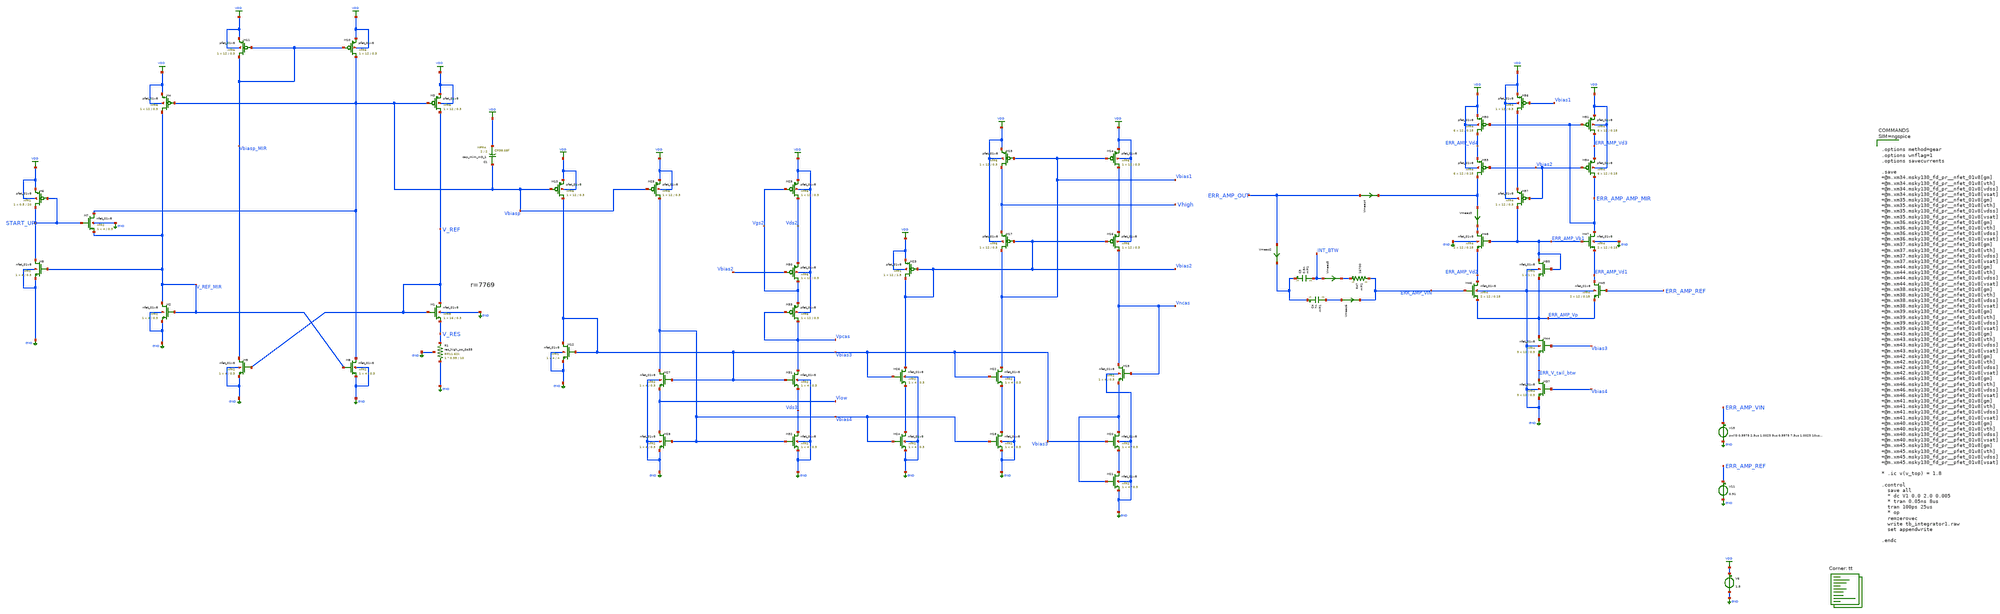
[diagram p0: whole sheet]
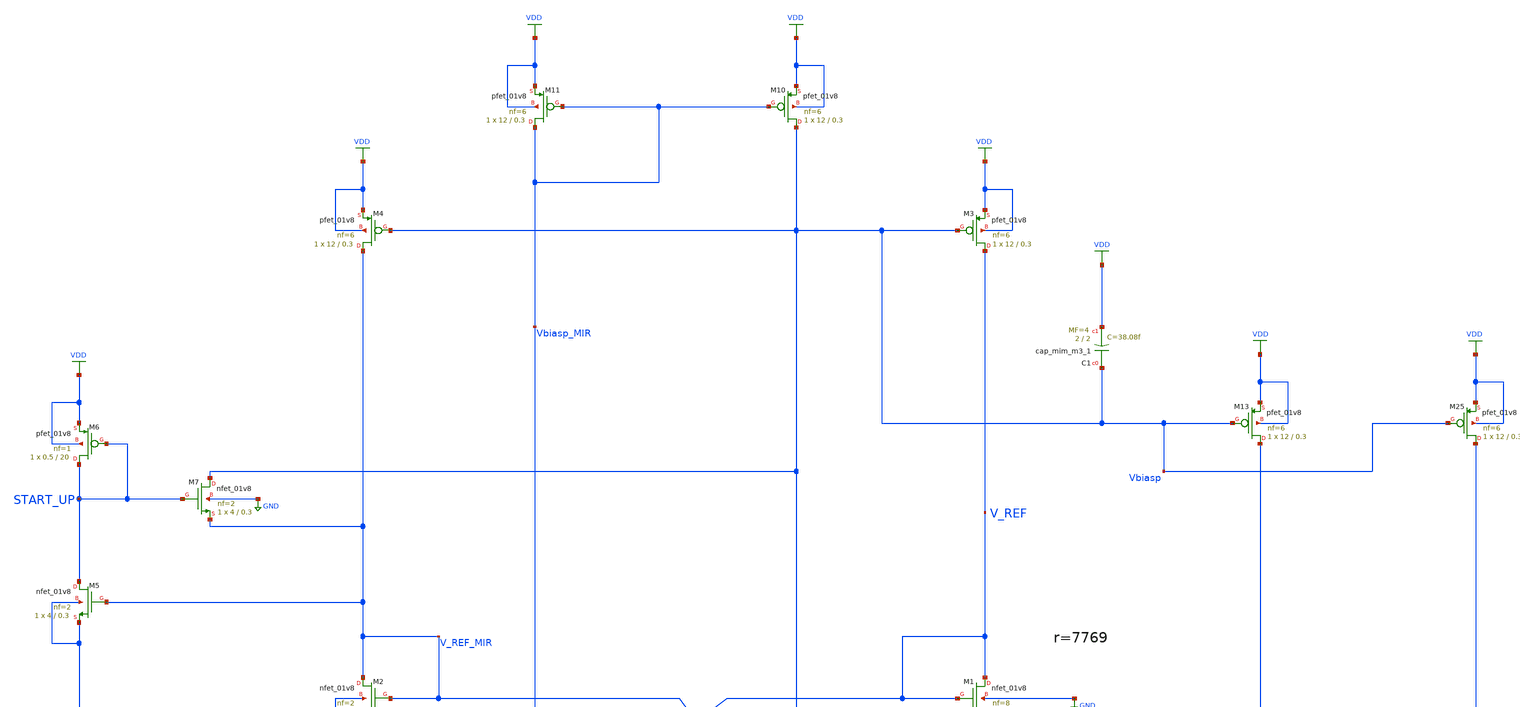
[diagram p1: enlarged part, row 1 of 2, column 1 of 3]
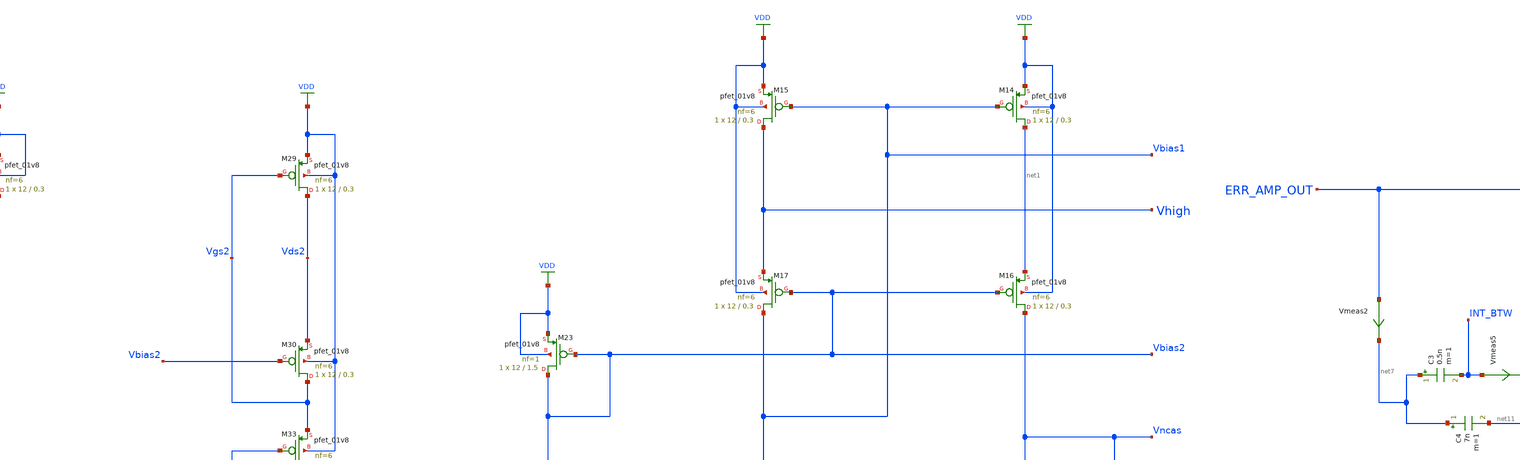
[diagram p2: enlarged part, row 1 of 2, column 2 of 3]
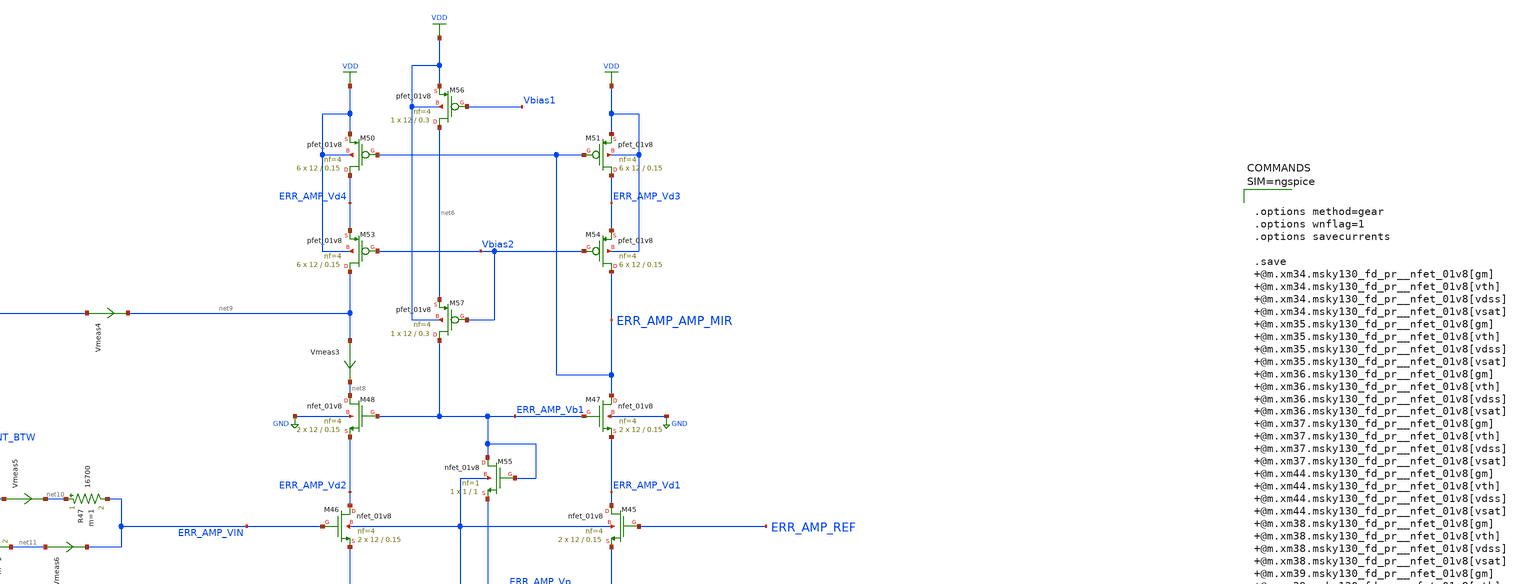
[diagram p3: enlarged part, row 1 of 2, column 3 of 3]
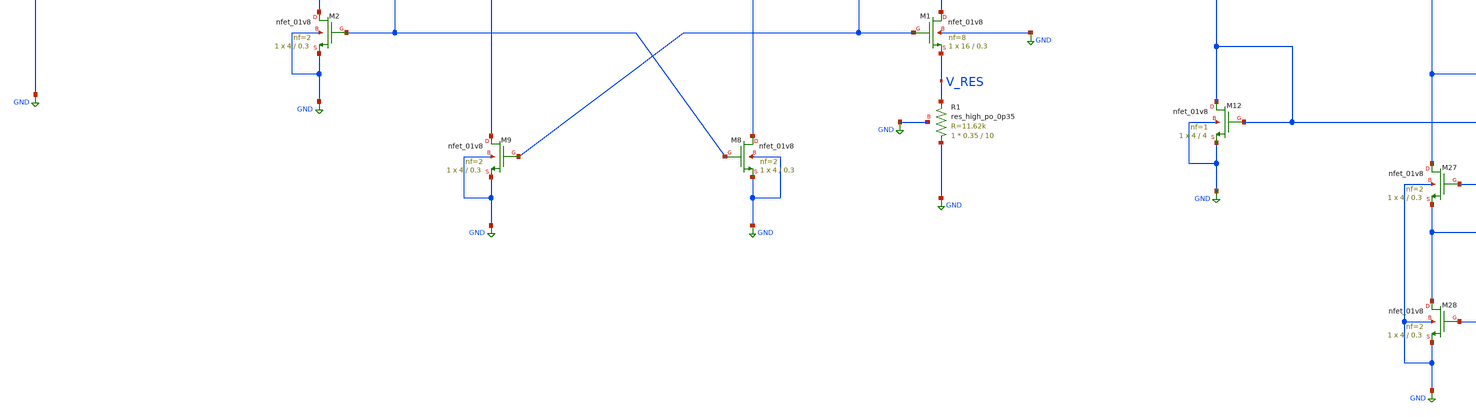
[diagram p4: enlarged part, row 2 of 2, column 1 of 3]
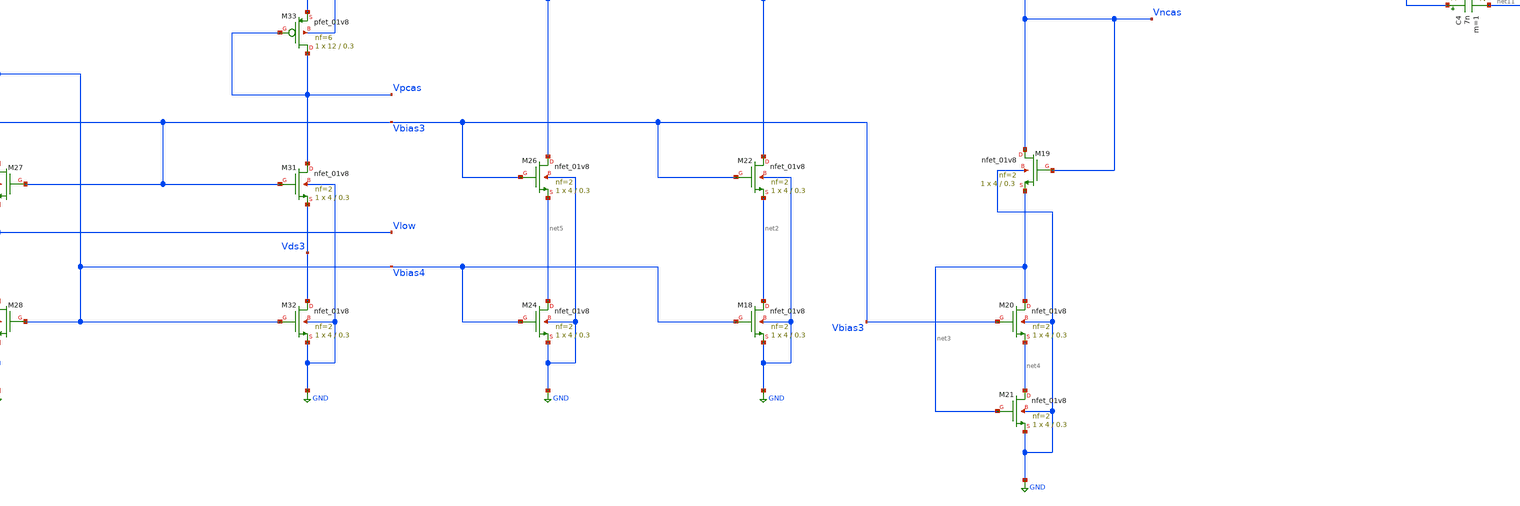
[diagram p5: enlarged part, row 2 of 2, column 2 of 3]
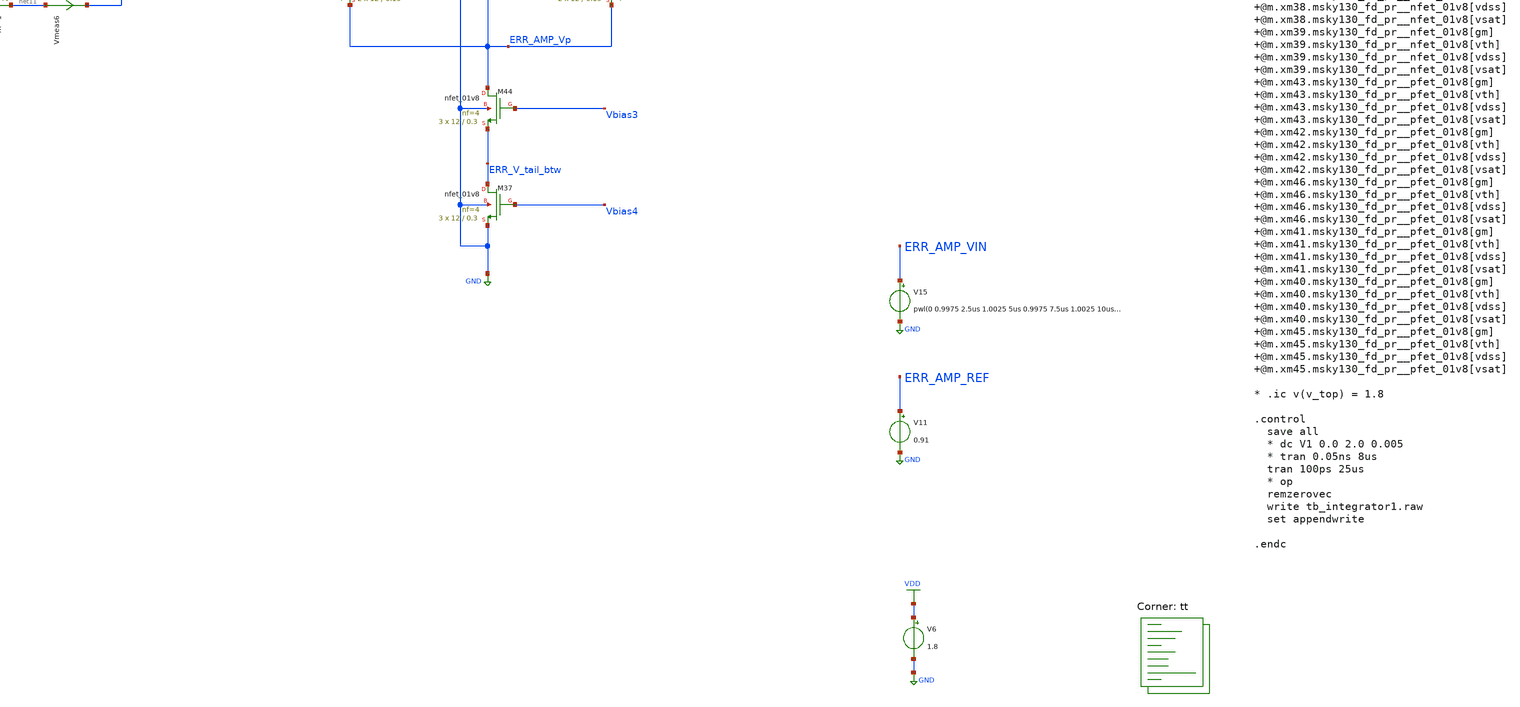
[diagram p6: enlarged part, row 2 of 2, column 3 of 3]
** sch_path: projects/ASU/EEE572/schematic/tb_integrator1.sch
**.subckt tb_integrator1
V6 VDD GND 1.8
XM1 V_REF V_REF V_RES GND sky130_fd_pr__nfet_01v8 L=0.3 W=16 nf=8 ad='int((nf+1)/2) * W/nf * 0.29' as='int((nf+2)/2) * W/nf * 0.29'
+ pd='2*int((nf+1)/2) * (W/nf + 0.29)' ps='2*int((nf+2)/2) * (W/nf + 0.29)' nrd='0.29 / W' nrs='0.29 / W'
+ sa=0 sb=0 sd=0 mult=1 m=1
XM2 V_REF_MIR V_REF_MIR GND GND sky130_fd_pr__nfet_01v8 L=0.3 W=4 nf=2 ad='int((nf+1)/2) * W/nf * 0.29'
+ as='int((nf+2)/2) * W/nf * 0.29' pd='2*int((nf+1)/2) * (W/nf + 0.29)' ps='2*int((nf+2)/2) * (W/nf + 0.29)'
+ nrd='0.29 / W' nrs='0.29 / W' sa=0 sb=0 sd=0 mult=1 m=1
XM5 START_UP V_REF_MIR GND GND sky130_fd_pr__nfet_01v8 L=0.3 W=4 nf=2 ad='int((nf+1)/2) * W/nf * 0.29'
+ as='int((nf+2)/2) * W/nf * 0.29' pd='2*int((nf+1)/2) * (W/nf + 0.29)' ps='2*int((nf+2)/2) * (W/nf + 0.29)'
+ nrd='0.29 / W' nrs='0.29 / W' sa=0 sb=0 sd=0 mult=1 m=1
XM7 Vbiasp START_UP V_REF_MIR GND sky130_fd_pr__nfet_01v8 L=0.3 W=4 nf=2 ad='int((nf+1)/2) * W/nf * 0.29'
+ as='int((nf+2)/2) * W/nf * 0.29' pd='2*int((nf+1)/2) * (W/nf + 0.29)' ps='2*int((nf+2)/2) * (W/nf + 0.29)'
+ nrd='0.29 / W' nrs='0.29 / W' sa=0 sb=0 sd=0 mult=1 m=1
XM6 START_UP START_UP VDD VDD sky130_fd_pr__pfet_01v8 L=20 W=0.5 nf=1 ad='int((nf+1)/2) * W/nf * 0.29'
+ as='int((nf+2)/2) * W/nf * 0.29' pd='2*int((nf+1)/2) * (W/nf + 0.29)' ps='2*int((nf+2)/2) * (W/nf + 0.29)'
+ nrd='0.29 / W' nrs='0.29 / W' sa=0 sb=0 sd=0 mult=1 m=1
XM3 V_REF Vbiasp VDD VDD sky130_fd_pr__pfet_01v8 L=0.3 W=12 nf=6 ad='int((nf+1)/2) * W/nf * 0.29' as='int((nf+2)/2) * W/nf * 0.29'
+ pd='2*int((nf+1)/2) * (W/nf + 0.29)' ps='2*int((nf+2)/2) * (W/nf + 0.29)' nrd='0.29 / W' nrs='0.29 / W'
+ sa=0 sb=0 sd=0 mult=1 m=1
XM4 V_REF_MIR Vbiasp VDD VDD sky130_fd_pr__pfet_01v8 L=0.3 W=12 nf=6 ad='int((nf+1)/2) * W/nf * 0.29'
+ as='int((nf+2)/2) * W/nf * 0.29' pd='2*int((nf+1)/2) * (W/nf + 0.29)' ps='2*int((nf+2)/2) * (W/nf + 0.29)'
+ nrd='0.29 / W' nrs='0.29 / W' sa=0 sb=0 sd=0 mult=1 m=1
XM8 Vbiasp V_REF_MIR GND GND sky130_fd_pr__nfet_01v8 L=0.3 W=4 nf=2 ad='int((nf+1)/2) * W/nf * 0.29'
+ as='int((nf+2)/2) * W/nf * 0.29' pd='2*int((nf+1)/2) * (W/nf + 0.29)' ps='2*int((nf+2)/2) * (W/nf + 0.29)'
+ nrd='0.29 / W' nrs='0.29 / W' sa=0 sb=0 sd=0 mult=1 m=1
XM9 Vbiasp_MIR V_REF GND GND sky130_fd_pr__nfet_01v8 L=0.3 W=4 nf=2 ad='int((nf+1)/2) * W/nf * 0.29'
+ as='int((nf+2)/2) * W/nf * 0.29' pd='2*int((nf+1)/2) * (W/nf + 0.29)' ps='2*int((nf+2)/2) * (W/nf + 0.29)'
+ nrd='0.29 / W' nrs='0.29 / W' sa=0 sb=0 sd=0 mult=1 m=1
XM10 Vbiasp Vbiasp_MIR VDD VDD sky130_fd_pr__pfet_01v8 L=0.3 W=12 nf=6 ad='int((nf+1)/2) * W/nf * 0.29'
+ as='int((nf+2)/2) * W/nf * 0.29' pd='2*int((nf+1)/2) * (W/nf + 0.29)' ps='2*int((nf+2)/2) * (W/nf + 0.29)'
+ nrd='0.29 / W' nrs='0.29 / W' sa=0 sb=0 sd=0 mult=1 m=1
XM11 Vbiasp_MIR Vbiasp_MIR VDD VDD sky130_fd_pr__pfet_01v8 L=0.3 W=12 nf=6 ad='int((nf+1)/2) * W/nf * 0.29'
+ as='int((nf+2)/2) * W/nf * 0.29' pd='2*int((nf+1)/2) * (W/nf + 0.29)' ps='2*int((nf+2)/2) * (W/nf + 0.29)'
+ nrd='0.29 / W' nrs='0.29 / W' sa=0 sb=0 sd=0 mult=1 m=1
XM12 Vbias3 Vbias3 GND GND sky130_fd_pr__nfet_01v8 L=4 W=4 nf=1 ad='int((nf+1)/2) * W/nf * 0.29' as='int((nf+2)/2) * W/nf * 0.29'
+ pd='2*int((nf+1)/2) * (W/nf + 0.29)' ps='2*int((nf+2)/2) * (W/nf + 0.29)' nrd='0.29 / W' nrs='0.29 / W'
+ sa=0 sb=0 sd=0 mult=1 m=1
XM13 Vbias3 Vbiasp VDD VDD sky130_fd_pr__pfet_01v8 L=0.3 W=12 nf=6 ad='int((nf+1)/2) * W/nf * 0.29' as='int((nf+2)/2) * W/nf * 0.29'
+ pd='2*int((nf+1)/2) * (W/nf + 0.29)' ps='2*int((nf+2)/2) * (W/nf + 0.29)' nrd='0.29 / W' nrs='0.29 / W'
+ sa=0 sb=0 sd=0 mult=1 m=1
XM14 net1 Vbias1 VDD VDD sky130_fd_pr__pfet_01v8 L=0.3 W=12 nf=6 ad='int((nf+1)/2) * W/nf * 0.29' as='int((nf+2)/2) * W/nf * 0.29'
+ pd='2*int((nf+1)/2) * (W/nf + 0.29)' ps='2*int((nf+2)/2) * (W/nf + 0.29)' nrd='0.29 / W' nrs='0.29 / W'
+ sa=0 sb=0 sd=0 mult=1 m=1
XM15 Vhigh Vbias1 VDD VDD sky130_fd_pr__pfet_01v8 L=0.3 W=12 nf=6 ad='int((nf+1)/2) * W/nf * 0.29' as='int((nf+2)/2) * W/nf * 0.29'
+ pd='2*int((nf+1)/2) * (W/nf + 0.29)' ps='2*int((nf+2)/2) * (W/nf + 0.29)' nrd='0.29 / W' nrs='0.29 / W'
+ sa=0 sb=0 sd=0 mult=1 m=1
XM16 Vncas Vbias2 net1 VDD sky130_fd_pr__pfet_01v8 L=0.3 W=12 nf=6 ad='int((nf+1)/2) * W/nf * 0.29' as='int((nf+2)/2) * W/nf * 0.29'
+ pd='2*int((nf+1)/2) * (W/nf + 0.29)' ps='2*int((nf+2)/2) * (W/nf + 0.29)' nrd='0.29 / W' nrs='0.29 / W'
+ sa=0 sb=0 sd=0 mult=1 m=1
XM17 Vbias1 Vbias2 Vhigh VDD sky130_fd_pr__pfet_01v8 L=0.3 W=12 nf=6 ad='int((nf+1)/2) * W/nf * 0.29'
+ as='int((nf+2)/2) * W/nf * 0.29' pd='2*int((nf+1)/2) * (W/nf + 0.29)' ps='2*int((nf+2)/2) * (W/nf + 0.29)'
+ nrd='0.29 / W' nrs='0.29 / W' sa=0 sb=0 sd=0 mult=1 m=1
XM18 net2 Vbias4 GND GND sky130_fd_pr__nfet_01v8 L=0.3 W=4 nf=2 ad='int((nf+1)/2) * W/nf * 0.29' as='int((nf+2)/2) * W/nf * 0.29'
+ pd='2*int((nf+1)/2) * (W/nf + 0.29)' ps='2*int((nf+2)/2) * (W/nf + 0.29)' nrd='0.29 / W' nrs='0.29 / W'
+ sa=0 sb=0 sd=0 mult=1 m=1
XM19 Vncas Vncas net3 GND sky130_fd_pr__nfet_01v8 L=0.3 W=4 nf=2 ad='int((nf+1)/2) * W/nf * 0.29' as='int((nf+2)/2) * W/nf * 0.29'
+ pd='2*int((nf+1)/2) * (W/nf + 0.29)' ps='2*int((nf+2)/2) * (W/nf + 0.29)' nrd='0.29 / W' nrs='0.29 / W'
+ sa=0 sb=0 sd=0 mult=1 m=1
XM20 net3 Vbias3 net4 GND sky130_fd_pr__nfet_01v8 L=0.3 W=4 nf=2 ad='int((nf+1)/2) * W/nf * 0.29' as='int((nf+2)/2) * W/nf * 0.29'
+ pd='2*int((nf+1)/2) * (W/nf + 0.29)' ps='2*int((nf+2)/2) * (W/nf + 0.29)' nrd='0.29 / W' nrs='0.29 / W'
+ sa=0 sb=0 sd=0 mult=1 m=1
XM21 net4 net3 GND GND sky130_fd_pr__nfet_01v8 L=0.3 W=4 nf=2 ad='int((nf+1)/2) * W/nf * 0.29' as='int((nf+2)/2) * W/nf * 0.29'
+ pd='2*int((nf+1)/2) * (W/nf + 0.29)' ps='2*int((nf+2)/2) * (W/nf + 0.29)' nrd='0.29 / W' nrs='0.29 / W'
+ sa=0 sb=0 sd=0 mult=1 m=1
XM25 Vbias4 Vbiasp VDD VDD sky130_fd_pr__pfet_01v8 L=0.3 W=12 nf=6 ad='int((nf+1)/2) * W/nf * 0.29' as='int((nf+2)/2) * W/nf * 0.29'
+ pd='2*int((nf+1)/2) * (W/nf + 0.29)' ps='2*int((nf+2)/2) * (W/nf + 0.29)' nrd='0.29 / W' nrs='0.29 / W'
+ sa=0 sb=0 sd=0 mult=1 m=1
XM27 Vbias4 Vbias3 Vlow GND sky130_fd_pr__nfet_01v8 L=0.3 W=4 nf=2 ad='int((nf+1)/2) * W/nf * 0.29' as='int((nf+2)/2) * W/nf * 0.29'
+ pd='2*int((nf+1)/2) * (W/nf + 0.29)' ps='2*int((nf+2)/2) * (W/nf + 0.29)' nrd='0.29 / W' nrs='0.29 / W'
+ sa=0 sb=0 sd=0 mult=1 m=1
XM28 Vlow Vbias4 GND GND sky130_fd_pr__nfet_01v8 L=0.3 W=4 nf=2 ad='int((nf+1)/2) * W/nf * 0.29' as='int((nf+2)/2) * W/nf * 0.29'
+ pd='2*int((nf+1)/2) * (W/nf + 0.29)' ps='2*int((nf+2)/2) * (W/nf + 0.29)' nrd='0.29 / W' nrs='0.29 / W'
+ sa=0 sb=0 sd=0 mult=1 m=1
XM29 Vds2 Vgs2 VDD VDD sky130_fd_pr__pfet_01v8 L=0.3 W=12 nf=6 ad='int((nf+1)/2) * W/nf * 0.29' as='int((nf+2)/2) * W/nf * 0.29'
+ pd='2*int((nf+1)/2) * (W/nf + 0.29)' ps='2*int((nf+2)/2) * (W/nf + 0.29)' nrd='0.29 / W' nrs='0.29 / W'
+ sa=0 sb=0 sd=0 mult=1 m=1
XM30 Vgs2 Vbias2 Vds2 VDD sky130_fd_pr__pfet_01v8 L=0.3 W=12 nf=6 ad='int((nf+1)/2) * W/nf * 0.29' as='int((nf+2)/2) * W/nf * 0.29'
+ pd='2*int((nf+1)/2) * (W/nf + 0.29)' ps='2*int((nf+2)/2) * (W/nf + 0.29)' nrd='0.29 / W' nrs='0.29 / W'
+ sa=0 sb=0 sd=0 mult=1 m=1
XM31 Vpcas Vbias3 Vds3 GND sky130_fd_pr__nfet_01v8 L=0.3 W=4 nf=2 ad='int((nf+1)/2) * W/nf * 0.29' as='int((nf+2)/2) * W/nf * 0.29'
+ pd='2*int((nf+1)/2) * (W/nf + 0.29)' ps='2*int((nf+2)/2) * (W/nf + 0.29)' nrd='0.29 / W' nrs='0.29 / W'
+ sa=0 sb=0 sd=0 mult=1 m=1
XM32 Vds3 Vbias4 GND GND sky130_fd_pr__nfet_01v8 L=0.3 W=4 nf=2 ad='int((nf+1)/2) * W/nf * 0.29' as='int((nf+2)/2) * W/nf * 0.29'
+ pd='2*int((nf+1)/2) * (W/nf + 0.29)' ps='2*int((nf+2)/2) * (W/nf + 0.29)' nrd='0.29 / W' nrs='0.29 / W'
+ sa=0 sb=0 sd=0 mult=1 m=1
XM33 Vpcas Vpcas Vgs2 VDD sky130_fd_pr__pfet_01v8 L=0.3 W=12 nf=6 ad='int((nf+1)/2) * W/nf * 0.29' as='int((nf+2)/2) * W/nf * 0.29'
+ pd='2*int((nf+1)/2) * (W/nf + 0.29)' ps='2*int((nf+2)/2) * (W/nf + 0.29)' nrd='0.29 / W' nrs='0.29 / W'
+ sa=0 sb=0 sd=0 mult=1 m=1
XM22 Vbias1 Vbias3 net2 GND sky130_fd_pr__nfet_01v8 L=0.3 W=4 nf=2 ad='int((nf+1)/2) * W/nf * 0.29' as='int((nf+2)/2) * W/nf * 0.29'
+ pd='2*int((nf+1)/2) * (W/nf + 0.29)' ps='2*int((nf+2)/2) * (W/nf + 0.29)' nrd='0.29 / W' nrs='0.29 / W'
+ sa=0 sb=0 sd=0 mult=1 m=1
XM23 Vbias2 Vbias2 VDD VDD sky130_fd_pr__pfet_01v8 L=1.5 W=12 nf=1 ad='int((nf+1)/2) * W/nf * 0.29' as='int((nf+2)/2) * W/nf * 0.29'
+ pd='2*int((nf+1)/2) * (W/nf + 0.29)' ps='2*int((nf+2)/2) * (W/nf + 0.29)' nrd='0.29 / W' nrs='0.29 / W'
+ sa=0 sb=0 sd=0 mult=1 m=1
XM24 net5 Vbias4 GND GND sky130_fd_pr__nfet_01v8 L=0.3 W=4 nf=2 ad='int((nf+1)/2) * W/nf * 0.29' as='int((nf+2)/2) * W/nf * 0.29'
+ pd='2*int((nf+1)/2) * (W/nf + 0.29)' ps='2*int((nf+2)/2) * (W/nf + 0.29)' nrd='0.29 / W' nrs='0.29 / W'
+ sa=0 sb=0 sd=0 mult=1 m=1
XM26 Vbias2 Vbias3 net5 GND sky130_fd_pr__nfet_01v8 L=0.3 W=4 nf=2 ad='int((nf+1)/2) * W/nf * 0.29' as='int((nf+2)/2) * W/nf * 0.29'
+ pd='2*int((nf+1)/2) * (W/nf + 0.29)' ps='2*int((nf+2)/2) * (W/nf + 0.29)' nrd='0.29 / W' nrs='0.29 / W'
+ sa=0 sb=0 sd=0 mult=1 m=1
XC1 Vbiasp VDD sky130_fd_pr__cap_mim_m3_1 W=2 L=2 MF=4 m=4
XR1 GND V_RES GND sky130_fd_pr__res_high_po_0p35 L=10 mult=1 m=1
XM37 ERR_V_tail_btw Vbias4 GND GND sky130_fd_pr__nfet_01v8 L=0.3 W=12 nf=4 ad='int((nf+1)/2) * W/nf * 0.29'
+ as='int((nf+2)/2) * W/nf * 0.29' pd='2*int((nf+1)/2) * (W/nf + 0.29)' ps='2*int((nf+2)/2) * (W/nf + 0.29)'
+ nrd='0.29 / W' nrs='0.29 / W' sa=0 sb=0 sd=0 mult=3 m=3
XM44 ERR_AMP_Vp Vbias3 ERR_V_tail_btw GND sky130_fd_pr__nfet_01v8 L=0.3 W=12 nf=4 ad='int((nf+1)/2) * W/nf * 0.29'
+ as='int((nf+2)/2) * W/nf * 0.29' pd='2*int((nf+1)/2) * (W/nf + 0.29)' ps='2*int((nf+2)/2) * (W/nf + 0.29)'
+ nrd='0.29 / W' nrs='0.29 / W' sa=0 sb=0 sd=0 mult=3 m=3
XM45 ERR_AMP_Vd1 ERR_AMP_REF ERR_AMP_Vp GND sky130_fd_pr__nfet_01v8 L=0.15 W=12 nf=4 ad='int((nf+1)/2) * W/nf * 0.29'
+ as='int((nf+2)/2) * W/nf * 0.29' pd='2*int((nf+1)/2) * (W/nf + 0.29)' ps='2*int((nf+2)/2) * (W/nf + 0.29)'
+ nrd='0.29 / W' nrs='0.29 / W' sa=0 sb=0 sd=0 mult=2 m=2
XM46 ERR_AMP_Vd2 ERR_AMP_VIN ERR_AMP_Vp GND sky130_fd_pr__nfet_01v8 L=0.15 W=12 nf=4 ad='int((nf+1)/2) * W/nf * 0.29'
+ as='int((nf+2)/2) * W/nf * 0.29' pd='2*int((nf+1)/2) * (W/nf + 0.29)' ps='2*int((nf+2)/2) * (W/nf + 0.29)'
+ nrd='0.29 / W' nrs='0.29 / W' sa=0 sb=0 sd=0 mult=2 m=2
XM47 ERR_AMP_AMP_MIR ERR_AMP_Vb1 ERR_AMP_Vd1 GND sky130_fd_pr__nfet_01v8 L=0.15 W=12 nf=4 ad='int((nf+1)/2) * W/nf * 0.29'
+ as='int((nf+2)/2) * W/nf * 0.29' pd='2*int((nf+1)/2) * (W/nf + 0.29)' ps='2*int((nf+2)/2) * (W/nf + 0.29)'
+ nrd='0.29 / W' nrs='0.29 / W' sa=0 sb=0 sd=0 mult=2 m=2
XM48 net8 ERR_AMP_Vb1 ERR_AMP_Vd2 GND sky130_fd_pr__nfet_01v8 L=0.15 W=12 nf=4 ad='int((nf+1)/2) * W/nf * 0.29'
+ as='int((nf+2)/2) * W/nf * 0.29' pd='2*int((nf+1)/2) * (W/nf + 0.29)' ps='2*int((nf+2)/2) * (W/nf + 0.29)'
+ nrd='0.29 / W' nrs='0.29 / W' sa=0 sb=0 sd=0 mult=2 m=2
XM50 ERR_AMP_Vd4 ERR_AMP_AMP_MIR VDD VDD sky130_fd_pr__pfet_01v8 L=0.15 W=12 nf=4 ad='int((nf+1)/2) * W/nf * 0.29'
+ as='int((nf+2)/2) * W/nf * 0.29' pd='2*int((nf+1)/2) * (W/nf + 0.29)' ps='2*int((nf+2)/2) * (W/nf + 0.29)'
+ nrd='0.29 / W' nrs='0.29 / W' sa=0 sb=0 sd=0 mult=6 m=6
XM51 ERR_AMP_Vd3 ERR_AMP_AMP_MIR VDD VDD sky130_fd_pr__pfet_01v8 L=0.15 W=12 nf=4 ad='int((nf+1)/2) * W/nf * 0.29'
+ as='int((nf+2)/2) * W/nf * 0.29' pd='2*int((nf+1)/2) * (W/nf + 0.29)' ps='2*int((nf+2)/2) * (W/nf + 0.29)'
+ nrd='0.29 / W' nrs='0.29 / W' sa=0 sb=0 sd=0 mult=6 m=6
XM53 net9 Vbias2 ERR_AMP_Vd4 VDD sky130_fd_pr__pfet_01v8 L=0.15 W=12 nf=4 ad='int((nf+1)/2) * W/nf * 0.29'
+ as='int((nf+2)/2) * W/nf * 0.29' pd='2*int((nf+1)/2) * (W/nf + 0.29)' ps='2*int((nf+2)/2) * (W/nf + 0.29)'
+ nrd='0.29 / W' nrs='0.29 / W' sa=0 sb=0 sd=0 mult=6 m=6
XM54 ERR_AMP_AMP_MIR Vbias2 ERR_AMP_Vd3 VDD sky130_fd_pr__pfet_01v8 L=0.15 W=12 nf=4 ad='int((nf+1)/2) * W/nf * 0.29'
+ as='int((nf+2)/2) * W/nf * 0.29' pd='2*int((nf+1)/2) * (W/nf + 0.29)' ps='2*int((nf+2)/2) * (W/nf + 0.29)'
+ nrd='0.29 / W' nrs='0.29 / W' sa=0 sb=0 sd=0 mult=6 m=6
XM55 ERR_AMP_Vb1 ERR_AMP_Vb1 ERR_AMP_Vp GND sky130_fd_pr__nfet_01v8 L=1 W=1 nf=1 ad='int((nf+1)/2) * W/nf * 0.29'
+ as='int((nf+2)/2) * W/nf * 0.29' pd='2*int((nf+1)/2) * (W/nf + 0.29)' ps='2*int((nf+2)/2) * (W/nf + 0.29)'
+ nrd='0.29 / W' nrs='0.29 / W' sa=0 sb=0 sd=0 mult=1 m=1
XM56 net6 Vbias1 VDD VDD sky130_fd_pr__pfet_01v8 L=0.3 W=12 nf=4 ad='int((nf+1)/2) * W/nf * 0.29' as='int((nf+2)/2) * W/nf * 0.29'
+ pd='2*int((nf+1)/2) * (W/nf + 0.29)' ps='2*int((nf+2)/2) * (W/nf + 0.29)' nrd='0.29 / W' nrs='0.29 / W'
+ sa=0 sb=0 sd=0 mult=1 m=1
XM57 ERR_AMP_Vb1 Vbias2 net6 VDD sky130_fd_pr__pfet_01v8 L=0.3 W=12 nf=4 ad='int((nf+1)/2) * W/nf * 0.29'
+ as='int((nf+2)/2) * W/nf * 0.29' pd='2*int((nf+1)/2) * (W/nf + 0.29)' ps='2*int((nf+2)/2) * (W/nf + 0.29)'
+ nrd='0.29 / W' nrs='0.29 / W' sa=0 sb=0 sd=0 mult=1 m=1
C3 net7 INT_BTW 0.5n m=1
R47 net10 ERR_AMP_VIN 16700 m=1
C4 net7 net11 7n m=1
V11 ERR_AMP_REF GND 0.91
V15 ERR_AMP_VIN GND pwl(0 0.9975 2.5us 1.0025 5us 0.9975 7.5us 1.0025 10us 0.9975 12.5us 1.0025 15us
+ 0.9975 17.5us 1.0025 20us 0.9975 22.5us 1.0025 25us 0.9975)
Vmeas2 ERR_AMP_OUT net7 0
.save i(vmeas2)
Vmeas3 net9 net8 0
.save i(vmeas3)
Vmeas4 ERR_AMP_OUT net9 0
.save i(vmeas4)
Vmeas5 INT_BTW net10 0
.save i(vmeas5)
Vmeas6 net11 ERR_AMP_VIN 0
.save i(vmeas6)
**** begin user architecture code
.lib $::SKYWATER_MODELS/sky130.lib.spice tt



.options method=gear
.options wnflag=1
.options savecurrents

.save @m.xm34.msky130_fd_pr__nfet_01v8[gm] @m.xm34.msky130_fd_pr__nfet_01v8[vth] @m.xm34.msky130_fd_pr__nfet_01v8[vdss] @m.xm34.msky130_fd_pr__nfet_01v8[vsat] @m.xm35.msky130_fd_pr__nfet_01v8[gm] @m.xm35.msky130_fd_pr__nfet_01v8[vth] @m.xm35.msky130_fd_pr__nfet_01v8[vdss] @m.xm35.msky130_fd_pr__nfet_01v8[vsat] @m.xm36.msky130_fd_pr__nfet_01v8[gm] @m.xm36.msky130_fd_pr__nfet_01v8[vth] @m.xm36.msky130_fd_pr__nfet_01v8[vdss] @m.xm36.msky130_fd_pr__nfet_01v8[vsat] @m.xm37.msky130_fd_pr__nfet_01v8[gm] @m.xm37.msky130_fd_pr__nfet_01v8[vth] @m.xm37.msky130_fd_pr__nfet_01v8[vdss] @m.xm37.msky130_fd_pr__nfet_01v8[vsat] @m.xm44.msky130_fd_pr__nfet_01v8[gm] @m.xm44.msky130_fd_pr__nfet_01v8[vth] @m.xm44.msky130_fd_pr__nfet_01v8[vdss] @m.xm44.msky130_fd_pr__nfet_01v8[vsat] @m.xm38.msky130_fd_pr__nfet_01v8[gm] @m.xm38.msky130_fd_pr__nfet_01v8[vth] @m.xm38.msky130_fd_pr__nfet_01v8[vdss] @m.xm38.msky130_fd_pr__nfet_01v8[vsat] @m.xm39.msky130_fd_pr__nfet_01v8[gm] @m.xm39.msky130_fd_pr__nfet_01v8[vth] @m.xm39.msky130_fd_pr__nfet_01v8[vdss] @m.xm39.msky130_fd_pr__nfet_01v8[vsat] @m.xm43.msky130_fd_pr__pfet_01v8[gm] @m.xm43.msky130_fd_pr__pfet_01v8[vth] @m.xm43.msky130_fd_pr__pfet_01v8[vdss] @m.xm43.msky130_fd_pr__pfet_01v8[vsat] @m.xm42.msky130_fd_pr__pfet_01v8[gm] @m.xm42.msky130_fd_pr__pfet_01v8[vth] @m.xm42.msky130_fd_pr__pfet_01v8[vdss] @m.xm42.msky130_fd_pr__pfet_01v8[vsat] @m.xm46.msky130_fd_pr__pfet_01v8[gm] @m.xm46.msky130_fd_pr__pfet_01v8[vth] @m.xm46.msky130_fd_pr__pfet_01v8[vdss] @m.xm46.msky130_fd_pr__pfet_01v8[vsat] @m.xm41.msky130_fd_pr__pfet_01v8[gm] @m.xm41.msky130_fd_pr__pfet_01v8[vth] @m.xm41.msky130_fd_pr__pfet_01v8[vdss] @m.xm41.msky130_fd_pr__pfet_01v8[vsat] @m.xm40.msky130_fd_pr__pfet_01v8[gm] @m.xm40.msky130_fd_pr__pfet_01v8[vth] @m.xm40.msky130_fd_pr__pfet_01v8[vdss] @m.xm40.msky130_fd_pr__pfet_01v8[vsat] @m.xm45.msky130_fd_pr__pfet_01v8[gm] @m.xm45.msky130_fd_pr__pfet_01v8[vth] @m.xm45.msky130_fd_pr__pfet_01v8[vdss] @m.xm45.msky130_fd_pr__pfet_01v8[vsat]

* .ic v(v_top) = 1.8

.control
  save all
  * dc V1 0.0 2.0 0.005
  * tran 0.05ns 8us
  tran 100ps 25us
  * op
  remzerovec
  write tb_integrator1.raw
  set appendwrite

.endc





**** end user architecture code
**.ends
.GLOBAL GND
.GLOBAL VDD
.end
